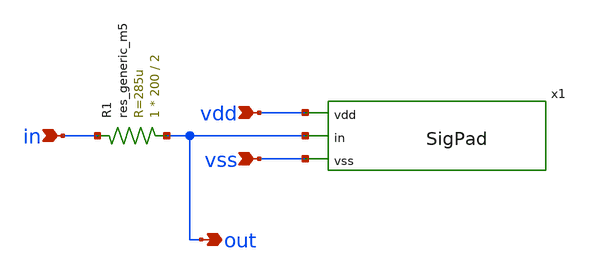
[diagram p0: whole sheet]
** sch_path: IO-cells/xschem/Padtest.sch
**.subckt Padtest in out vss vdd
*.ipin in
*.opin out
*.ipin vss
*.ipin vdd
R1 out in sky130_fd_pr__res_generic_m5 W=200 L=2 m=1
x1 vdd out vss SigPad
**.ends

* expanding   symbol:  SigPad.sym # of pins=3
** sym_path: IO-cells/xschem/SigPad.sym
** sch_path: IO-cells/xschem/SigPad.sch
.subckt SigPad vdd in vss
*.ipin in
*.ipin vdd
*.ipin vss
XD1 in vdd sky130_fd_pr__diode_pd2nw_05v5 area=1000e12 pj=4e6
XD2 vss in sky130_fd_pr__diode_pw2nd_05v5 area=1000e12 pj=4e6
.ends

.end
